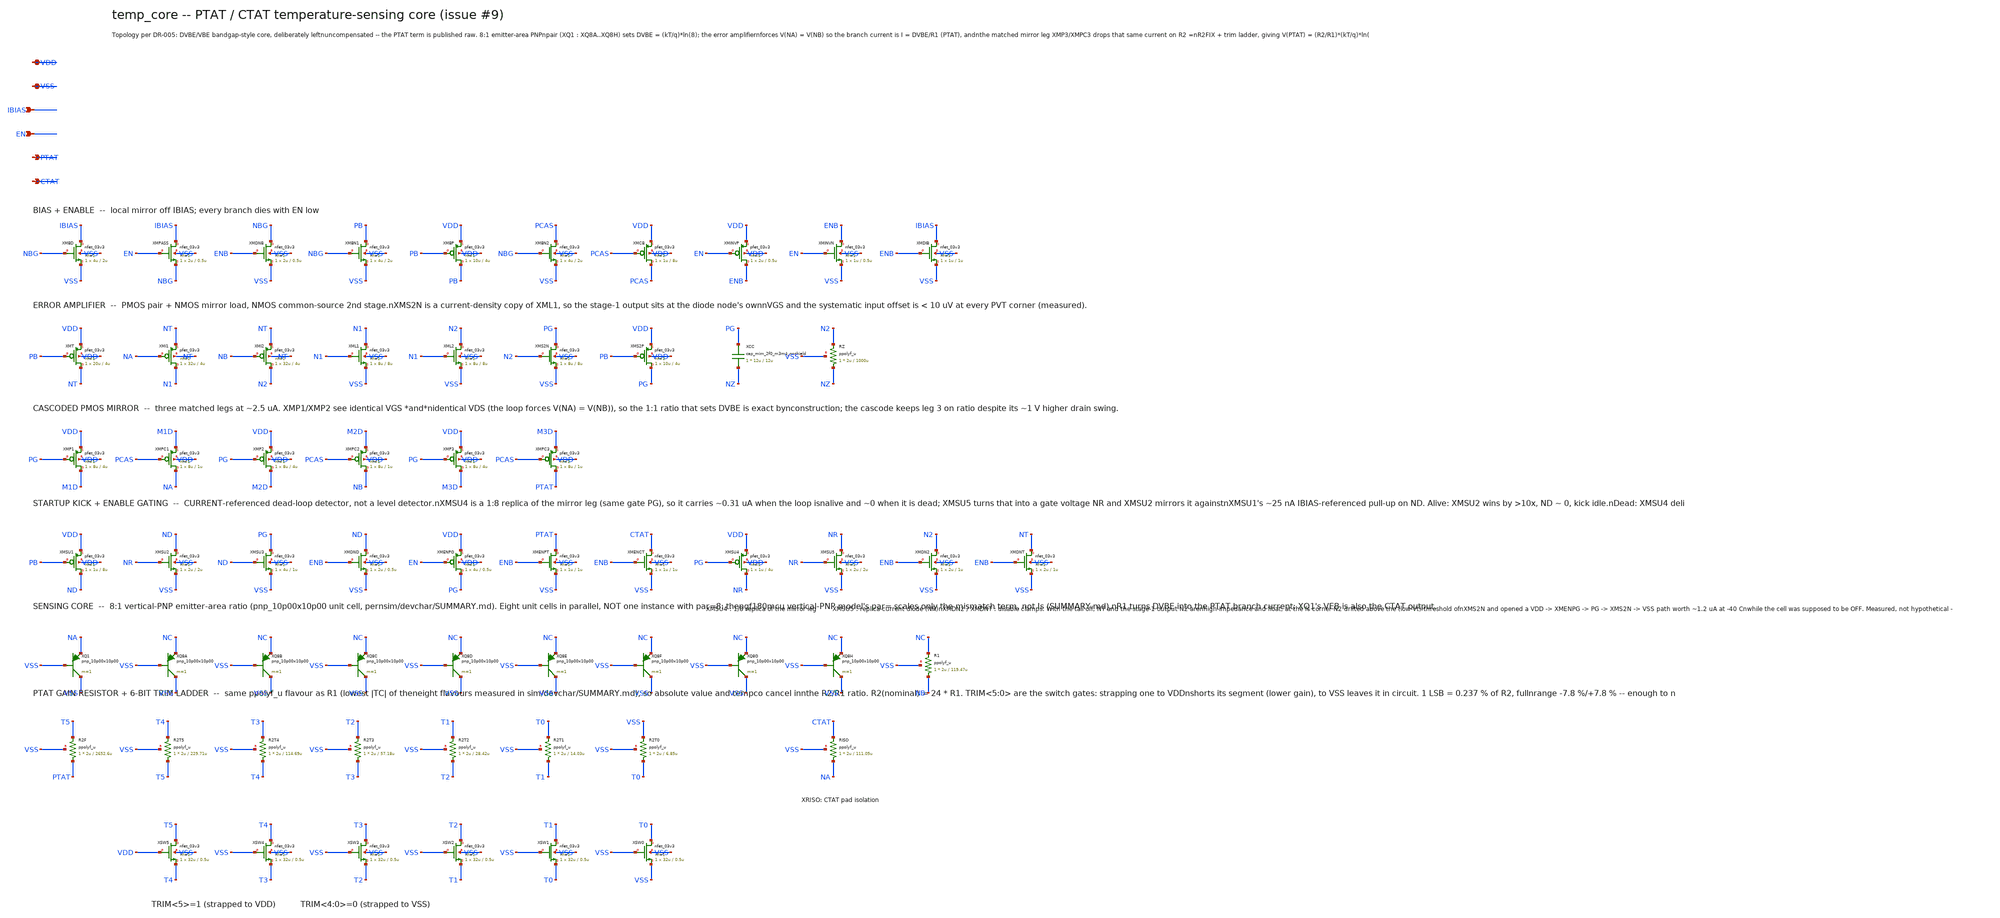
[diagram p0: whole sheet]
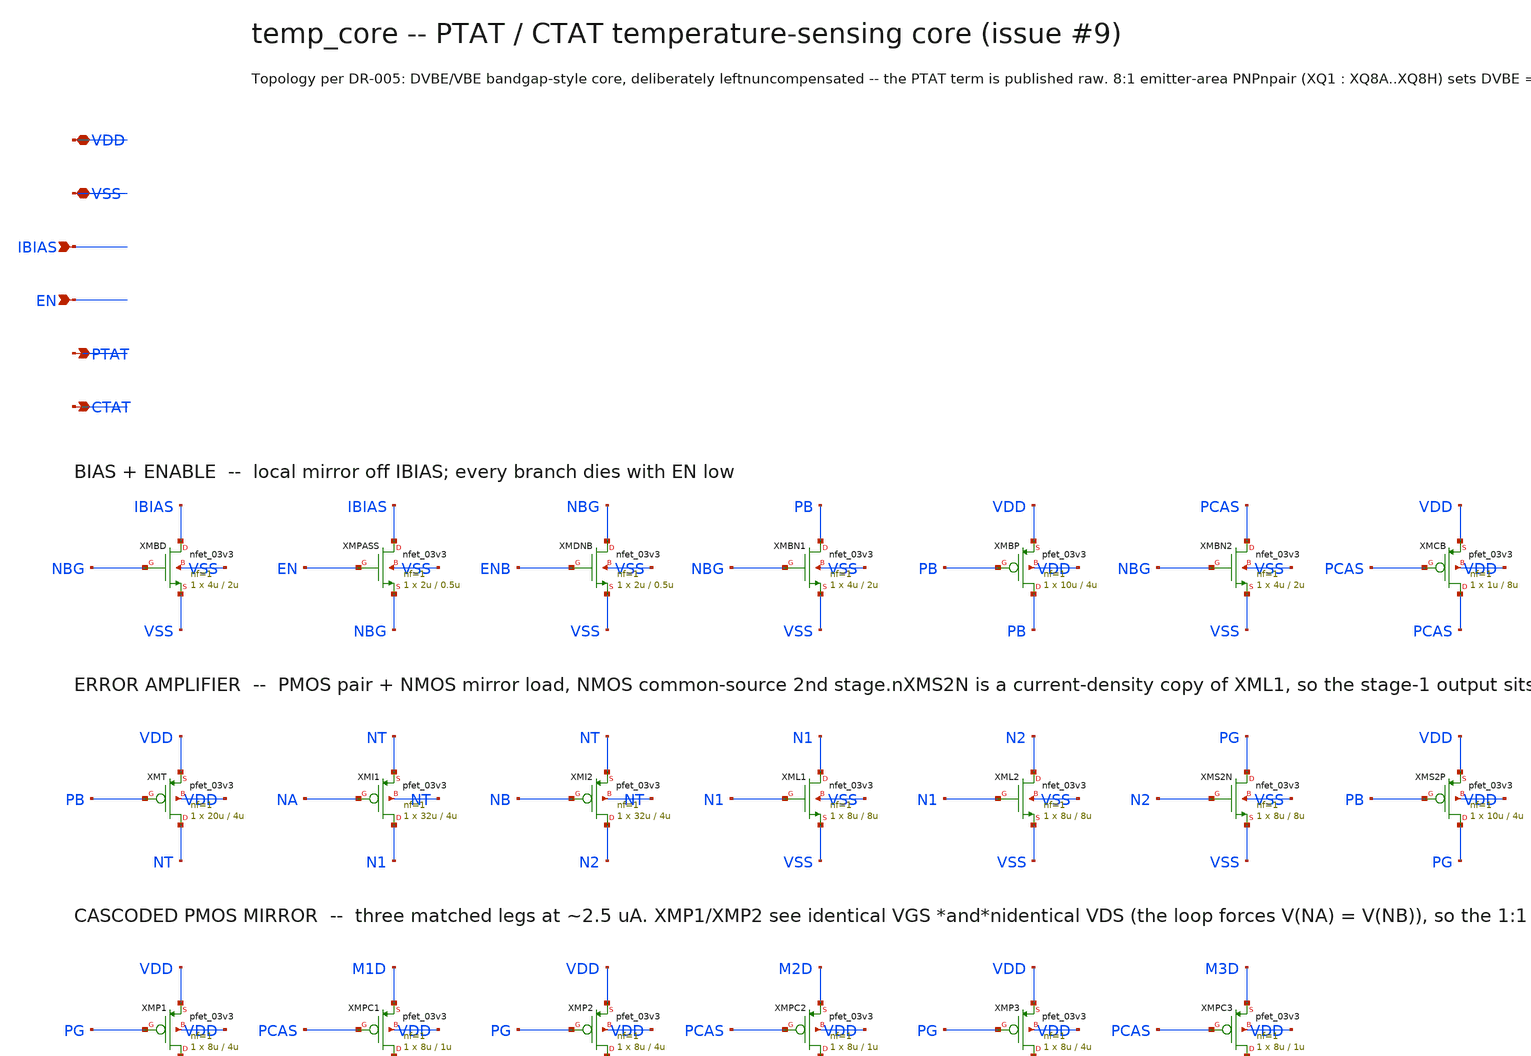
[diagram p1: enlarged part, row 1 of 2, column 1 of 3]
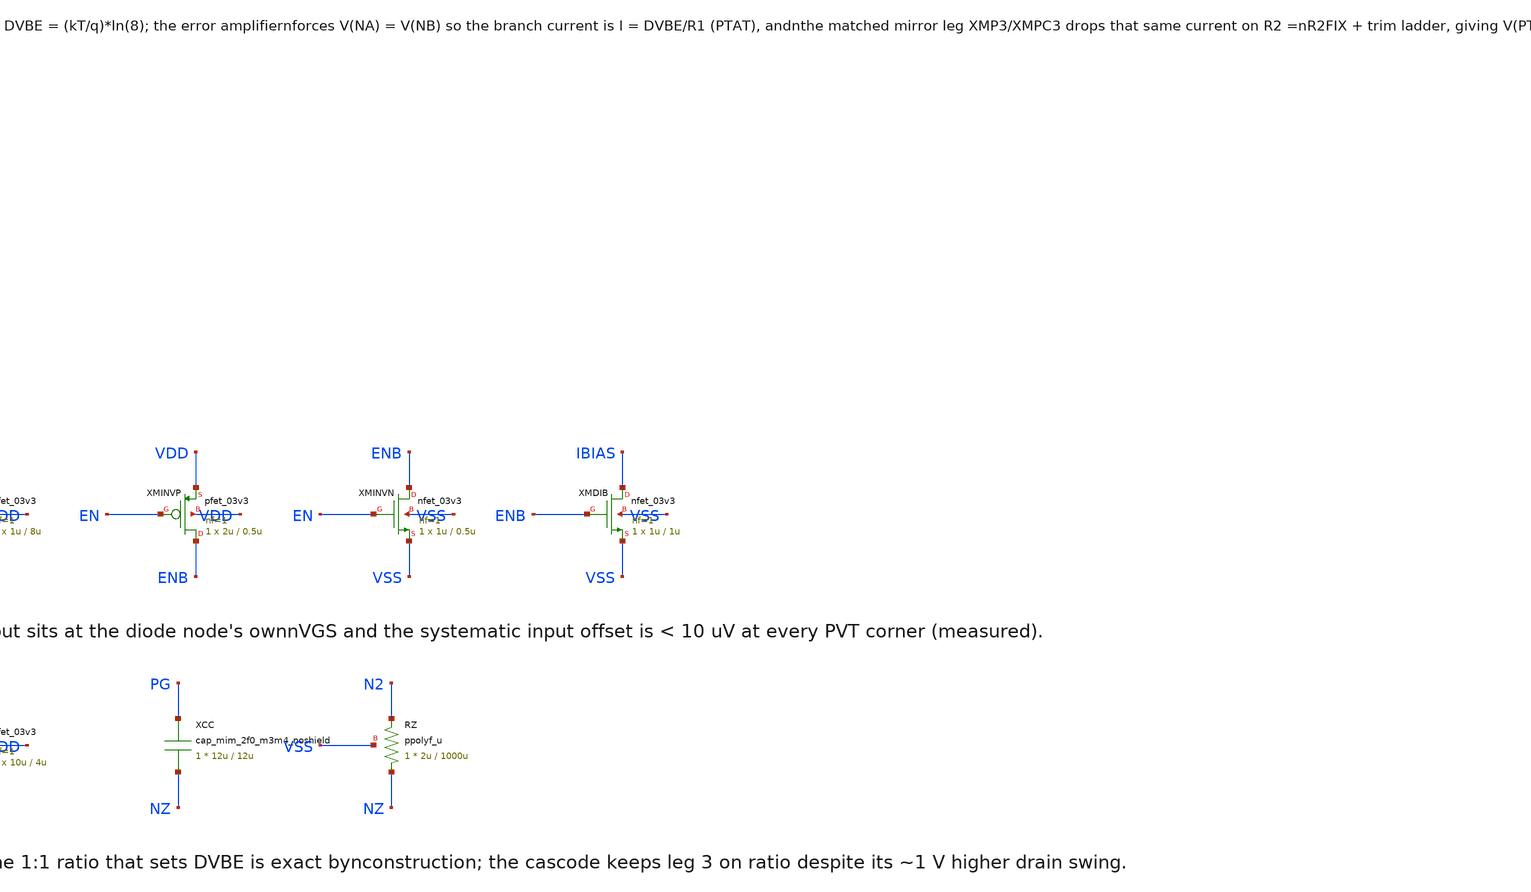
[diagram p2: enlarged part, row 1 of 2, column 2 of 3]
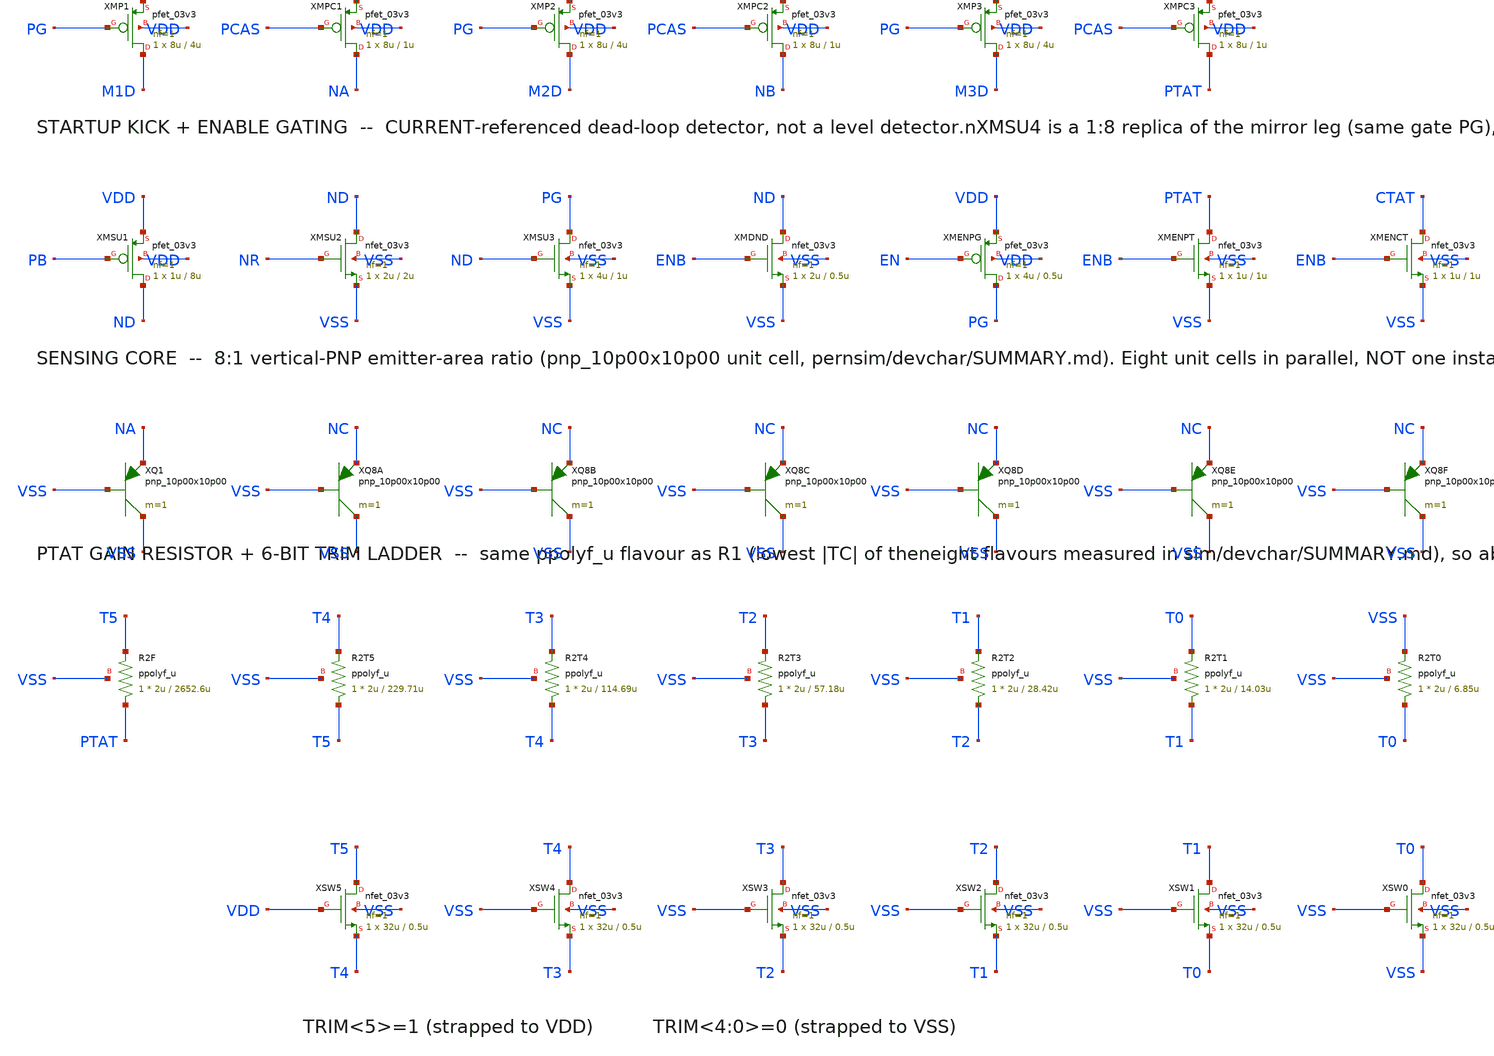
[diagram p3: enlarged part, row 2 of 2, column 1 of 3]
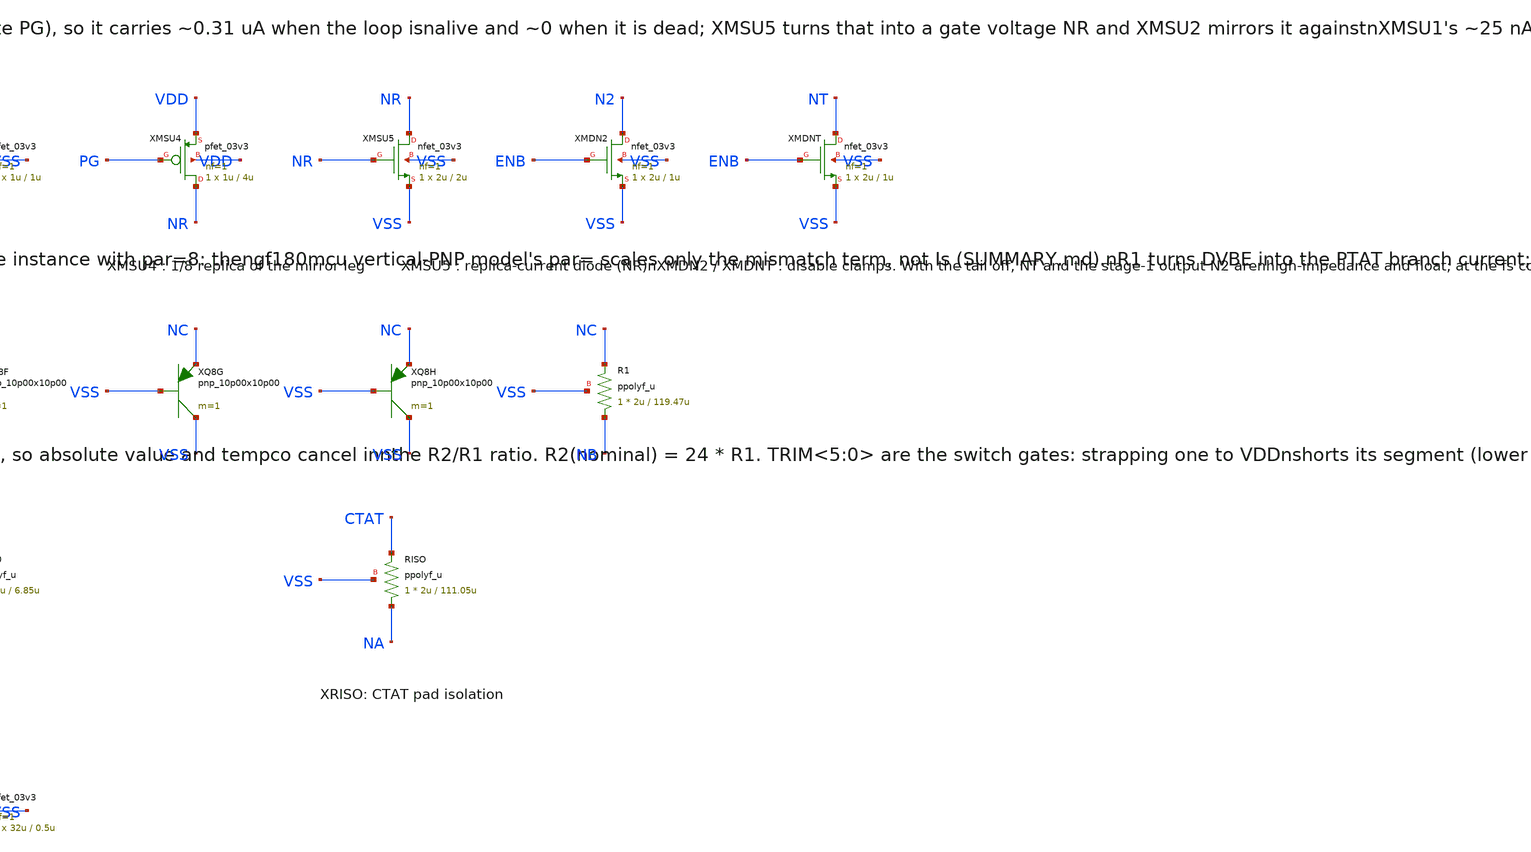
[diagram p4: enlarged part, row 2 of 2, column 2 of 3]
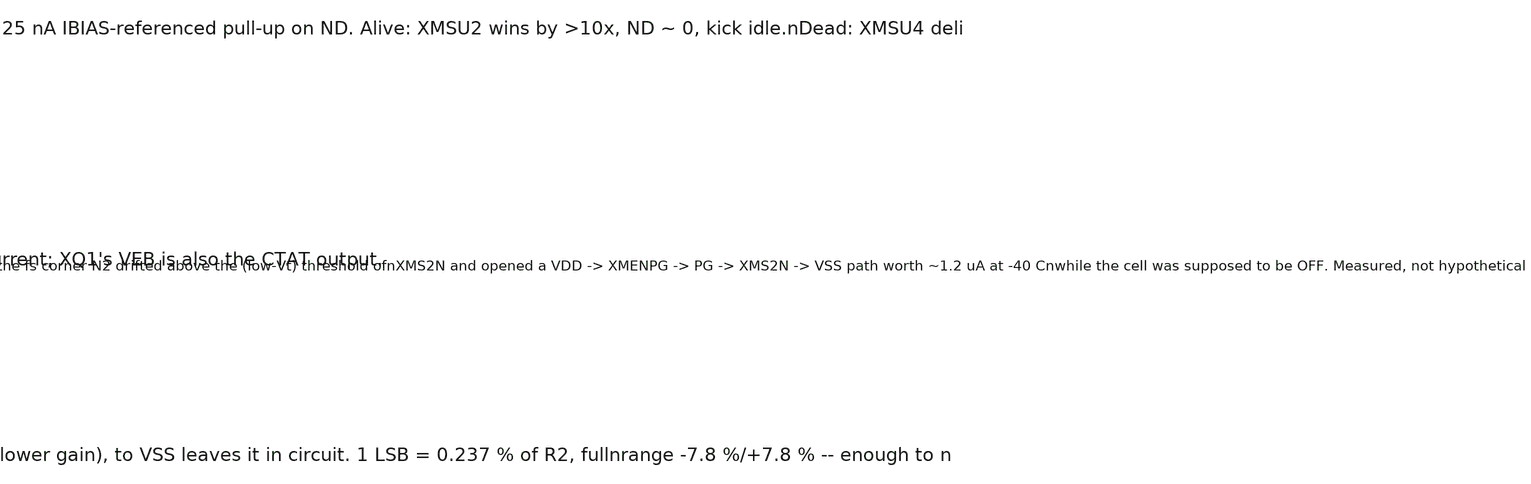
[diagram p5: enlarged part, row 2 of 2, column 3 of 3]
** sch_path: design/temp_core.sch
**.subckt temp_core VDD VSS IBIAS EN PTAT CTAT
*.iopin VDD
*.iopin VSS
*.ipin IBIAS
*.ipin EN
*.opin PTAT
*.opin CTAT
XMBD IBIAS NBG VSS VSS nfet_03v3 L=2u W=4u nf=1 ad='int((nf+1)/2) * W/nf * 0.18u' as='int((nf+2)/2) * W/nf * 0.18u'
+ pd='2*int((nf+1)/2) * (W/nf + 0.18u)' ps='2*int((nf+2)/2) * (W/nf + 0.18u)' nrd='0.18u / W' nrs='0.18u / W'
+ sa=0 sb=0 sd=0 m=1
XMPASS IBIAS EN NBG VSS nfet_03v3 L=0.5u W=2u nf=1 ad='int((nf+1)/2) * W/nf * 0.18u' as='int((nf+2)/2) * W/nf * 0.18u'
+ pd='2*int((nf+1)/2) * (W/nf + 0.18u)' ps='2*int((nf+2)/2) * (W/nf + 0.18u)' nrd='0.18u / W' nrs='0.18u / W'
+ sa=0 sb=0 sd=0 m=1
XMDNB NBG ENB VSS VSS nfet_03v3 L=0.5u W=2u nf=1 ad='int((nf+1)/2) * W/nf * 0.18u' as='int((nf+2)/2) * W/nf * 0.18u'
+ pd='2*int((nf+1)/2) * (W/nf + 0.18u)' ps='2*int((nf+2)/2) * (W/nf + 0.18u)' nrd='0.18u / W' nrs='0.18u / W'
+ sa=0 sb=0 sd=0 m=1
XMDIB IBIAS ENB VSS VSS nfet_03v3 L=1u W=1u nf=1 ad='int((nf+1)/2) * W/nf * 0.18u' as='int((nf+2)/2) * W/nf * 0.18u'
+ pd='2*int((nf+1)/2) * (W/nf + 0.18u)' ps='2*int((nf+2)/2) * (W/nf + 0.18u)' nrd='0.18u / W' nrs='0.18u / W'
+ sa=0 sb=0 sd=0 m=1
XMBN1 PB NBG VSS VSS nfet_03v3 L=2u W=4u nf=1 ad='int((nf+1)/2) * W/nf * 0.18u' as='int((nf+2)/2) * W/nf * 0.18u'
+ pd='2*int((nf+1)/2) * (W/nf + 0.18u)' ps='2*int((nf+2)/2) * (W/nf + 0.18u)' nrd='0.18u / W' nrs='0.18u / W'
+ sa=0 sb=0 sd=0 m=1
XMBP PB PB VDD VDD pfet_03v3 L=4u W=10u nf=1 ad='int((nf+1)/2) * W/nf * 0.18u' as='int((nf+2)/2) * W/nf * 0.18u'
+ pd='2*int((nf+1)/2) * (W/nf + 0.18u)' ps='2*int((nf+2)/2) * (W/nf + 0.18u)' nrd='0.18u / W' nrs='0.18u / W'
+ sa=0 sb=0 sd=0 m=1
XMBN2 PCAS NBG VSS VSS nfet_03v3 L=2u W=4u nf=1 ad='int((nf+1)/2) * W/nf * 0.18u' as='int((nf+2)/2) * W/nf * 0.18u'
+ pd='2*int((nf+1)/2) * (W/nf + 0.18u)' ps='2*int((nf+2)/2) * (W/nf + 0.18u)' nrd='0.18u / W' nrs='0.18u / W'
+ sa=0 sb=0 sd=0 m=1
XMCB PCAS PCAS VDD VDD pfet_03v3 L=8u W=1u nf=1 ad='int((nf+1)/2) * W/nf * 0.18u' as='int((nf+2)/2) * W/nf * 0.18u'
+ pd='2*int((nf+1)/2) * (W/nf + 0.18u)' ps='2*int((nf+2)/2) * (W/nf + 0.18u)' nrd='0.18u / W' nrs='0.18u / W'
+ sa=0 sb=0 sd=0 m=1
XMINVP ENB EN VDD VDD pfet_03v3 L=0.5u W=2u nf=1 ad='int((nf+1)/2) * W/nf * 0.18u' as='int((nf+2)/2) * W/nf * 0.18u'
+ pd='2*int((nf+1)/2) * (W/nf + 0.18u)' ps='2*int((nf+2)/2) * (W/nf + 0.18u)' nrd='0.18u / W' nrs='0.18u / W'
+ sa=0 sb=0 sd=0 m=1
XMINVN ENB EN VSS VSS nfet_03v3 L=0.5u W=1u nf=1 ad='int((nf+1)/2) * W/nf * 0.18u' as='int((nf+2)/2) * W/nf * 0.18u'
+ pd='2*int((nf+1)/2) * (W/nf + 0.18u)' ps='2*int((nf+2)/2) * (W/nf + 0.18u)' nrd='0.18u / W' nrs='0.18u / W'
+ sa=0 sb=0 sd=0 m=1
XMT NT PB VDD VDD pfet_03v3 L=4u W=20u nf=1 ad='int((nf+1)/2) * W/nf * 0.18u' as='int((nf+2)/2) * W/nf * 0.18u'
+ pd='2*int((nf+1)/2) * (W/nf + 0.18u)' ps='2*int((nf+2)/2) * (W/nf + 0.18u)' nrd='0.18u / W' nrs='0.18u / W'
+ sa=0 sb=0 sd=0 m=1
XMI1 N1 NA NT NT pfet_03v3 L=4u W=32u nf=1 ad='int((nf+1)/2) * W/nf * 0.18u' as='int((nf+2)/2) * W/nf * 0.18u'
+ pd='2*int((nf+1)/2) * (W/nf + 0.18u)' ps='2*int((nf+2)/2) * (W/nf + 0.18u)' nrd='0.18u / W' nrs='0.18u / W'
+ sa=0 sb=0 sd=0 m=1
XMI2 N2 NB NT NT pfet_03v3 L=4u W=32u nf=1 ad='int((nf+1)/2) * W/nf * 0.18u' as='int((nf+2)/2) * W/nf * 0.18u'
+ pd='2*int((nf+1)/2) * (W/nf + 0.18u)' ps='2*int((nf+2)/2) * (W/nf + 0.18u)' nrd='0.18u / W' nrs='0.18u / W'
+ sa=0 sb=0 sd=0 m=1
XML1 N1 N1 VSS VSS nfet_03v3 L=8u W=8u nf=1 ad='int((nf+1)/2) * W/nf * 0.18u' as='int((nf+2)/2) * W/nf * 0.18u'
+ pd='2*int((nf+1)/2) * (W/nf + 0.18u)' ps='2*int((nf+2)/2) * (W/nf + 0.18u)' nrd='0.18u / W' nrs='0.18u / W'
+ sa=0 sb=0 sd=0 m=1
XML2 N2 N1 VSS VSS nfet_03v3 L=8u W=8u nf=1 ad='int((nf+1)/2) * W/nf * 0.18u' as='int((nf+2)/2) * W/nf * 0.18u'
+ pd='2*int((nf+1)/2) * (W/nf + 0.18u)' ps='2*int((nf+2)/2) * (W/nf + 0.18u)' nrd='0.18u / W' nrs='0.18u / W'
+ sa=0 sb=0 sd=0 m=1
XMS2N PG N2 VSS VSS nfet_03v3 L=8u W=8u nf=1 ad='int((nf+1)/2) * W/nf * 0.18u' as='int((nf+2)/2) * W/nf * 0.18u'
+ pd='2*int((nf+1)/2) * (W/nf + 0.18u)' ps='2*int((nf+2)/2) * (W/nf + 0.18u)' nrd='0.18u / W' nrs='0.18u / W'
+ sa=0 sb=0 sd=0 m=1
XMS2P PG PB VDD VDD pfet_03v3 L=4u W=10u nf=1 ad='int((nf+1)/2) * W/nf * 0.18u' as='int((nf+2)/2) * W/nf * 0.18u'
+ pd='2*int((nf+1)/2) * (W/nf + 0.18u)' ps='2*int((nf+2)/2) * (W/nf + 0.18u)' nrd='0.18u / W' nrs='0.18u / W'
+ sa=0 sb=0 sd=0 m=1
XCC PG NZ cap_mim_2f0_m3m4_noshield c_width=12u c_length=12u m=1
XRZ NZ N2 VSS ppolyf_u r_width=2u r_length=1000u m=1
XMP1 M1D PG VDD VDD pfet_03v3 L=4u W=8u nf=1 ad='int((nf+1)/2) * W/nf * 0.18u' as='int((nf+2)/2) * W/nf * 0.18u'
+ pd='2*int((nf+1)/2) * (W/nf + 0.18u)' ps='2*int((nf+2)/2) * (W/nf + 0.18u)' nrd='0.18u / W' nrs='0.18u / W'
+ sa=0 sb=0 sd=0 m=1
XMPC1 NA PCAS M1D VDD pfet_03v3 L=1u W=8u nf=1 ad='int((nf+1)/2) * W/nf * 0.18u' as='int((nf+2)/2) * W/nf * 0.18u'
+ pd='2*int((nf+1)/2) * (W/nf + 0.18u)' ps='2*int((nf+2)/2) * (W/nf + 0.18u)' nrd='0.18u / W' nrs='0.18u / W'
+ sa=0 sb=0 sd=0 m=1
XMP2 M2D PG VDD VDD pfet_03v3 L=4u W=8u nf=1 ad='int((nf+1)/2) * W/nf * 0.18u' as='int((nf+2)/2) * W/nf * 0.18u'
+ pd='2*int((nf+1)/2) * (W/nf + 0.18u)' ps='2*int((nf+2)/2) * (W/nf + 0.18u)' nrd='0.18u / W' nrs='0.18u / W'
+ sa=0 sb=0 sd=0 m=1
XMPC2 NB PCAS M2D VDD pfet_03v3 L=1u W=8u nf=1 ad='int((nf+1)/2) * W/nf * 0.18u' as='int((nf+2)/2) * W/nf * 0.18u'
+ pd='2*int((nf+1)/2) * (W/nf + 0.18u)' ps='2*int((nf+2)/2) * (W/nf + 0.18u)' nrd='0.18u / W' nrs='0.18u / W'
+ sa=0 sb=0 sd=0 m=1
XMP3 M3D PG VDD VDD pfet_03v3 L=4u W=8u nf=1 ad='int((nf+1)/2) * W/nf * 0.18u' as='int((nf+2)/2) * W/nf * 0.18u'
+ pd='2*int((nf+1)/2) * (W/nf + 0.18u)' ps='2*int((nf+2)/2) * (W/nf + 0.18u)' nrd='0.18u / W' nrs='0.18u / W'
+ sa=0 sb=0 sd=0 m=1
XMPC3 PTAT PCAS M3D VDD pfet_03v3 L=1u W=8u nf=1 ad='int((nf+1)/2) * W/nf * 0.18u' as='int((nf+2)/2) * W/nf * 0.18u'
+ pd='2*int((nf+1)/2) * (W/nf + 0.18u)' ps='2*int((nf+2)/2) * (W/nf + 0.18u)' nrd='0.18u / W' nrs='0.18u / W'
+ sa=0 sb=0 sd=0 m=1
XMSU1 ND PB VDD VDD pfet_03v3 L=8u W=1u nf=1 ad='int((nf+1)/2) * W/nf * 0.18u' as='int((nf+2)/2) * W/nf * 0.18u'
+ pd='2*int((nf+1)/2) * (W/nf + 0.18u)' ps='2*int((nf+2)/2) * (W/nf + 0.18u)' nrd='0.18u / W' nrs='0.18u / W'
+ sa=0 sb=0 sd=0 m=1
XMSU2 ND NR VSS VSS nfet_03v3 L=2u W=2u nf=1 ad='int((nf+1)/2) * W/nf * 0.18u' as='int((nf+2)/2) * W/nf * 0.18u'
+ pd='2*int((nf+1)/2) * (W/nf + 0.18u)' ps='2*int((nf+2)/2) * (W/nf + 0.18u)' nrd='0.18u / W' nrs='0.18u / W'
+ sa=0 sb=0 sd=0 m=1
XMSU3 PG ND VSS VSS nfet_03v3 L=1u W=4u nf=1 ad='int((nf+1)/2) * W/nf * 0.18u' as='int((nf+2)/2) * W/nf * 0.18u'
+ pd='2*int((nf+1)/2) * (W/nf + 0.18u)' ps='2*int((nf+2)/2) * (W/nf + 0.18u)' nrd='0.18u / W' nrs='0.18u / W'
+ sa=0 sb=0 sd=0 m=1
XMDND ND ENB VSS VSS nfet_03v3 L=0.5u W=2u nf=1 ad='int((nf+1)/2) * W/nf * 0.18u' as='int((nf+2)/2) * W/nf * 0.18u'
+ pd='2*int((nf+1)/2) * (W/nf + 0.18u)' ps='2*int((nf+2)/2) * (W/nf + 0.18u)' nrd='0.18u / W' nrs='0.18u / W'
+ sa=0 sb=0 sd=0 m=1
XMENPG PG EN VDD VDD pfet_03v3 L=0.5u W=4u nf=1 ad='int((nf+1)/2) * W/nf * 0.18u' as='int((nf+2)/2) * W/nf * 0.18u'
+ pd='2*int((nf+1)/2) * (W/nf + 0.18u)' ps='2*int((nf+2)/2) * (W/nf + 0.18u)' nrd='0.18u / W' nrs='0.18u / W'
+ sa=0 sb=0 sd=0 m=1
XMENPT PTAT ENB VSS VSS nfet_03v3 L=1u W=1u nf=1 ad='int((nf+1)/2) * W/nf * 0.18u' as='int((nf+2)/2) * W/nf * 0.18u'
+ pd='2*int((nf+1)/2) * (W/nf + 0.18u)' ps='2*int((nf+2)/2) * (W/nf + 0.18u)' nrd='0.18u / W' nrs='0.18u / W'
+ sa=0 sb=0 sd=0 m=1
XMENCT CTAT ENB VSS VSS nfet_03v3 L=1u W=1u nf=1 ad='int((nf+1)/2) * W/nf * 0.18u' as='int((nf+2)/2) * W/nf * 0.18u'
+ pd='2*int((nf+1)/2) * (W/nf + 0.18u)' ps='2*int((nf+2)/2) * (W/nf + 0.18u)' nrd='0.18u / W' nrs='0.18u / W'
+ sa=0 sb=0 sd=0 m=1
XMSU4 NR PG VDD VDD pfet_03v3 L=4u W=1u nf=1 ad='int((nf+1)/2) * W/nf * 0.18u' as='int((nf+2)/2) * W/nf * 0.18u'
+ pd='2*int((nf+1)/2) * (W/nf + 0.18u)' ps='2*int((nf+2)/2) * (W/nf + 0.18u)' nrd='0.18u / W' nrs='0.18u / W'
+ sa=0 sb=0 sd=0 m=1
XMSU5 NR NR VSS VSS nfet_03v3 L=2u W=2u nf=1 ad='int((nf+1)/2) * W/nf * 0.18u' as='int((nf+2)/2) * W/nf * 0.18u'
+ pd='2*int((nf+1)/2) * (W/nf + 0.18u)' ps='2*int((nf+2)/2) * (W/nf + 0.18u)' nrd='0.18u / W' nrs='0.18u / W'
+ sa=0 sb=0 sd=0 m=1
XMDN2 N2 ENB VSS VSS nfet_03v3 L=1u W=2u nf=1 ad='int((nf+1)/2) * W/nf * 0.18u' as='int((nf+2)/2) * W/nf * 0.18u'
+ pd='2*int((nf+1)/2) * (W/nf + 0.18u)' ps='2*int((nf+2)/2) * (W/nf + 0.18u)' nrd='0.18u / W' nrs='0.18u / W'
+ sa=0 sb=0 sd=0 m=1
XMDNT NT ENB VSS VSS nfet_03v3 L=1u W=2u nf=1 ad='int((nf+1)/2) * W/nf * 0.18u' as='int((nf+2)/2) * W/nf * 0.18u'
+ pd='2*int((nf+1)/2) * (W/nf + 0.18u)' ps='2*int((nf+2)/2) * (W/nf + 0.18u)' nrd='0.18u / W' nrs='0.18u / W'
+ sa=0 sb=0 sd=0 m=1
XQ1 VSS VSS NA pnp_10p00x10p00 m=1
XQ8A VSS VSS NC pnp_10p00x10p00 m=1
XQ8B VSS VSS NC pnp_10p00x10p00 m=1
XQ8C VSS VSS NC pnp_10p00x10p00 m=1
XQ8D VSS VSS NC pnp_10p00x10p00 m=1
XQ8E VSS VSS NC pnp_10p00x10p00 m=1
XQ8F VSS VSS NC pnp_10p00x10p00 m=1
XQ8G VSS VSS NC pnp_10p00x10p00 m=1
XQ8H VSS VSS NC pnp_10p00x10p00 m=1
XR1 NB NC VSS ppolyf_u r_width=2u r_length=119.47u m=1
XR2F PTAT T5 VSS ppolyf_u r_width=2u r_length=2652.6u m=1
XR2T5 T5 T4 VSS ppolyf_u r_width=2u r_length=229.71u m=1
XR2T4 T4 T3 VSS ppolyf_u r_width=2u r_length=114.69u m=1
XR2T3 T3 T2 VSS ppolyf_u r_width=2u r_length=57.18u m=1
XR2T2 T2 T1 VSS ppolyf_u r_width=2u r_length=28.42u m=1
XR2T1 T1 T0 VSS ppolyf_u r_width=2u r_length=14.03u m=1
XR2T0 T0 VSS VSS ppolyf_u r_width=2u r_length=6.85u m=1
XRISO NA CTAT VSS ppolyf_u r_width=2u r_length=111.05u m=1
XSW5 T5 VDD T4 VSS nfet_03v3 L=0.5u W=32u nf=1 ad='int((nf+1)/2) * W/nf * 0.18u' as='int((nf+2)/2) * W/nf * 0.18u'
+ pd='2*int((nf+1)/2) * (W/nf + 0.18u)' ps='2*int((nf+2)/2) * (W/nf + 0.18u)' nrd='0.18u / W' nrs='0.18u / W'
+ sa=0 sb=0 sd=0 m=1
XSW4 T4 VSS T3 VSS nfet_03v3 L=0.5u W=32u nf=1 ad='int((nf+1)/2) * W/nf * 0.18u' as='int((nf+2)/2) * W/nf * 0.18u'
+ pd='2*int((nf+1)/2) * (W/nf + 0.18u)' ps='2*int((nf+2)/2) * (W/nf + 0.18u)' nrd='0.18u / W' nrs='0.18u / W'
+ sa=0 sb=0 sd=0 m=1
XSW3 T3 VSS T2 VSS nfet_03v3 L=0.5u W=32u nf=1 ad='int((nf+1)/2) * W/nf * 0.18u' as='int((nf+2)/2) * W/nf * 0.18u'
+ pd='2*int((nf+1)/2) * (W/nf + 0.18u)' ps='2*int((nf+2)/2) * (W/nf + 0.18u)' nrd='0.18u / W' nrs='0.18u / W'
+ sa=0 sb=0 sd=0 m=1
XSW2 T2 VSS T1 VSS nfet_03v3 L=0.5u W=32u nf=1 ad='int((nf+1)/2) * W/nf * 0.18u' as='int((nf+2)/2) * W/nf * 0.18u'
+ pd='2*int((nf+1)/2) * (W/nf + 0.18u)' ps='2*int((nf+2)/2) * (W/nf + 0.18u)' nrd='0.18u / W' nrs='0.18u / W'
+ sa=0 sb=0 sd=0 m=1
XSW1 T1 VSS T0 VSS nfet_03v3 L=0.5u W=32u nf=1 ad='int((nf+1)/2) * W/nf * 0.18u' as='int((nf+2)/2) * W/nf * 0.18u'
+ pd='2*int((nf+1)/2) * (W/nf + 0.18u)' ps='2*int((nf+2)/2) * (W/nf + 0.18u)' nrd='0.18u / W' nrs='0.18u / W'
+ sa=0 sb=0 sd=0 m=1
XSW0 T0 VSS VSS VSS nfet_03v3 L=0.5u W=32u nf=1 ad='int((nf+1)/2) * W/nf * 0.18u' as='int((nf+2)/2) * W/nf * 0.18u'
+ pd='2*int((nf+1)/2) * (W/nf + 0.18u)' ps='2*int((nf+2)/2) * (W/nf + 0.18u)' nrd='0.18u / W' nrs='0.18u / W'
+ sa=0 sb=0 sd=0 m=1
**.ends
.end
